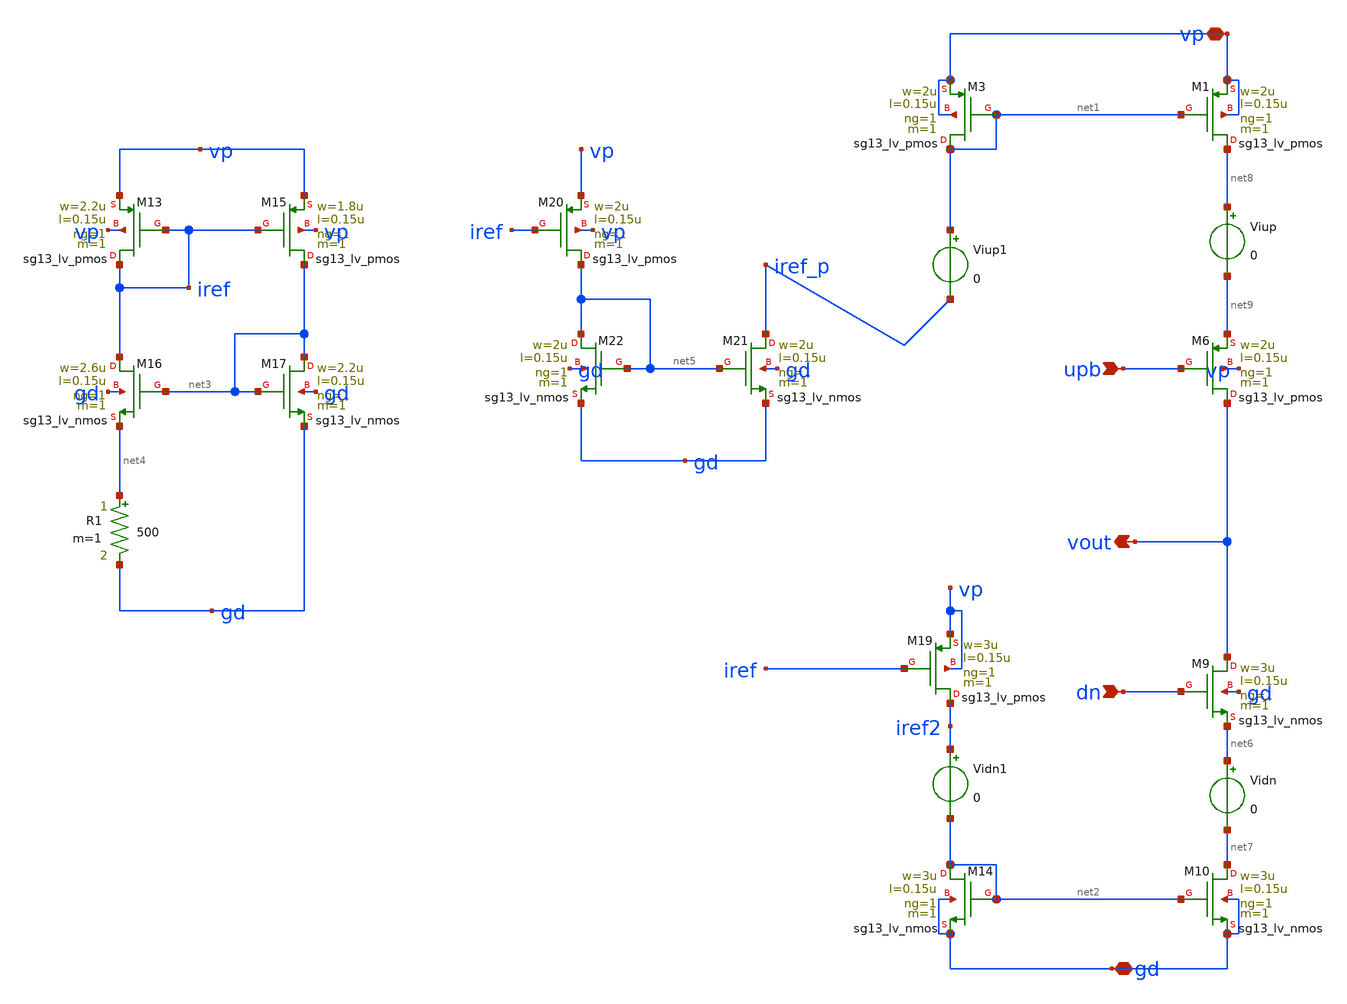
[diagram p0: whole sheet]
** sch_path: charge_pump/cp2_cs.sch
**.subckt cp2_cs vp upb vout dn gd
*.iopin vp
*.ipin upb
*.opin vout
*.ipin dn
*.iopin gd
XM3 net1 net1 vp vp sg13_lv_pmos w=2u l=0.15u ng=1 m=1 mm_ok=1
XM1 net8 net1 vp vp sg13_lv_pmos w=2u l=0.15u ng=1 m=1 mm_ok=1
XM6 vout upb net9 vp sg13_lv_pmos w=2u l=0.15u ng=1 m=1 mm_ok=1
XM9 vout dn net6 gd sg13_lv_nmos w=3u l=0.15u ng=1 m=1 mm_ok=1
XM10 net7 net2 gd gd sg13_lv_nmos w=3u l=0.15u ng=1 m=1 mm_ok=1
XM14 net2 net2 gd gd sg13_lv_nmos w=3u l=0.15u ng=1 m=1 mm_ok=1
XM13 iref iref vp vp sg13_lv_pmos w=2.2u l=0.15u ng=1 m=1 mm_ok=1
XM15 net3 iref vp vp sg13_lv_pmos w=1.8u l=0.15u ng=1 m=1 mm_ok=1
XM16 iref net3 net4 gd sg13_lv_nmos w=2.6u l=0.15u ng=1 m=1 mm_ok=1
XM17 net3 net3 gd gd sg13_lv_nmos w=2.2u l=0.15u ng=1 m=1 mm_ok=1
R1 net4 gd 500 m=1
XM20 net5 iref vp vp sg13_lv_pmos w=2u l=0.15u ng=1 m=1 mm_ok=1
XM21 iref_p net5 gd gd sg13_lv_nmos w=2u l=0.15u ng=1 m=1 mm_ok=1
XM22 net5 net5 gd gd sg13_lv_nmos w=2u l=0.15u ng=1 m=1 mm_ok=1
XM19 iref2 iref vp vp sg13_lv_pmos w=3u l=0.15u ng=1 m=1 mm_ok=1
Viup net8 net9 0
Vidn net6 net7 0
Viup1 net1 iref_p 0
Vidn1 iref2 net2 0
**.ends
.end
